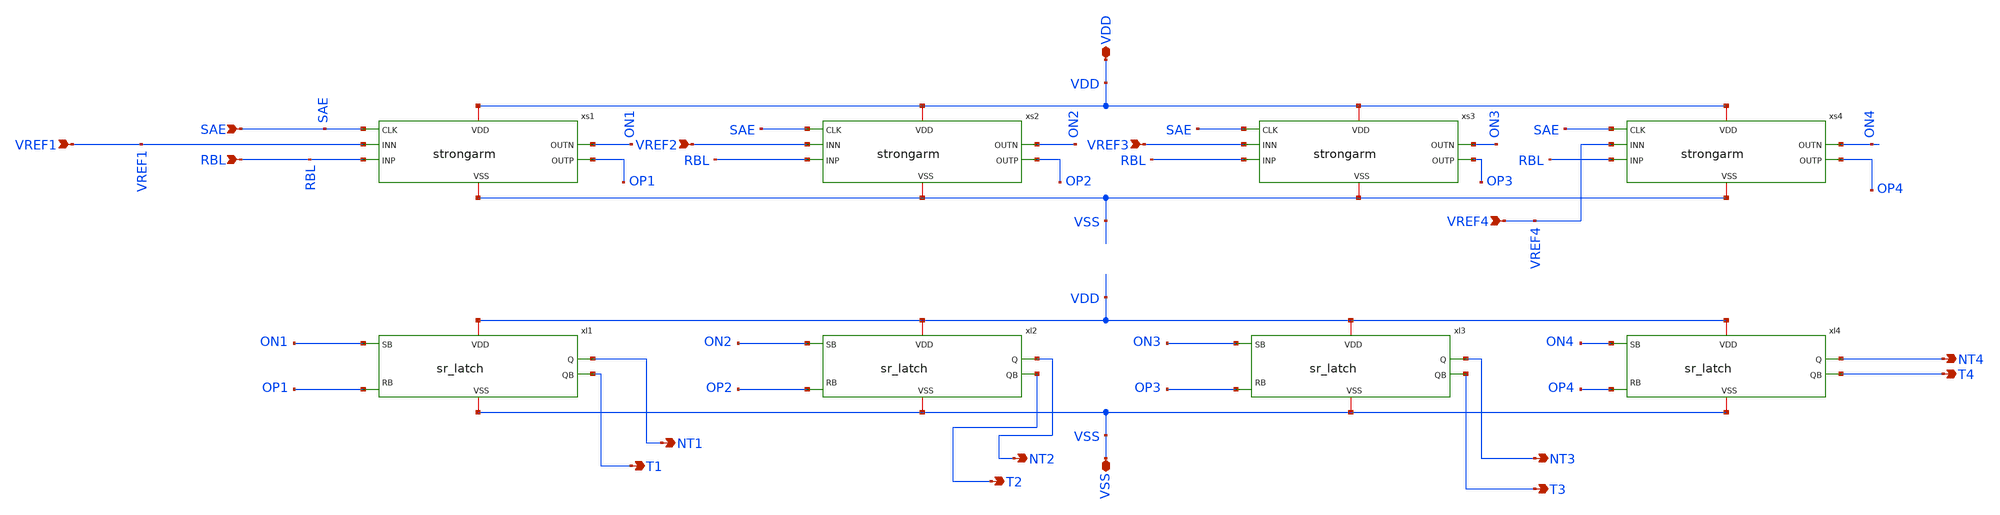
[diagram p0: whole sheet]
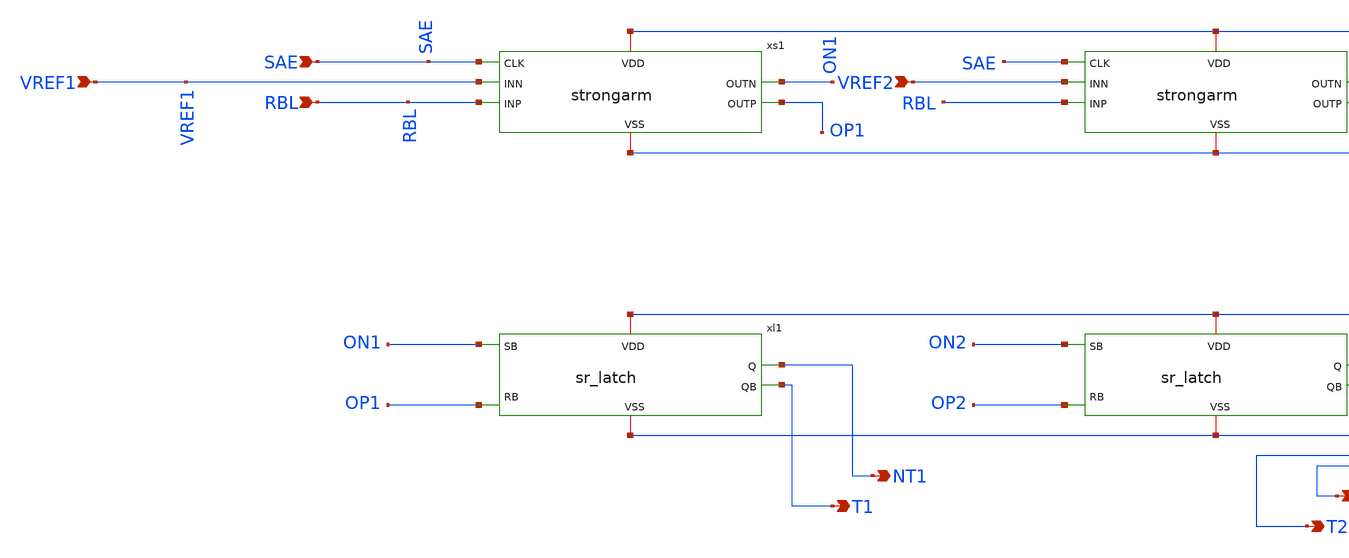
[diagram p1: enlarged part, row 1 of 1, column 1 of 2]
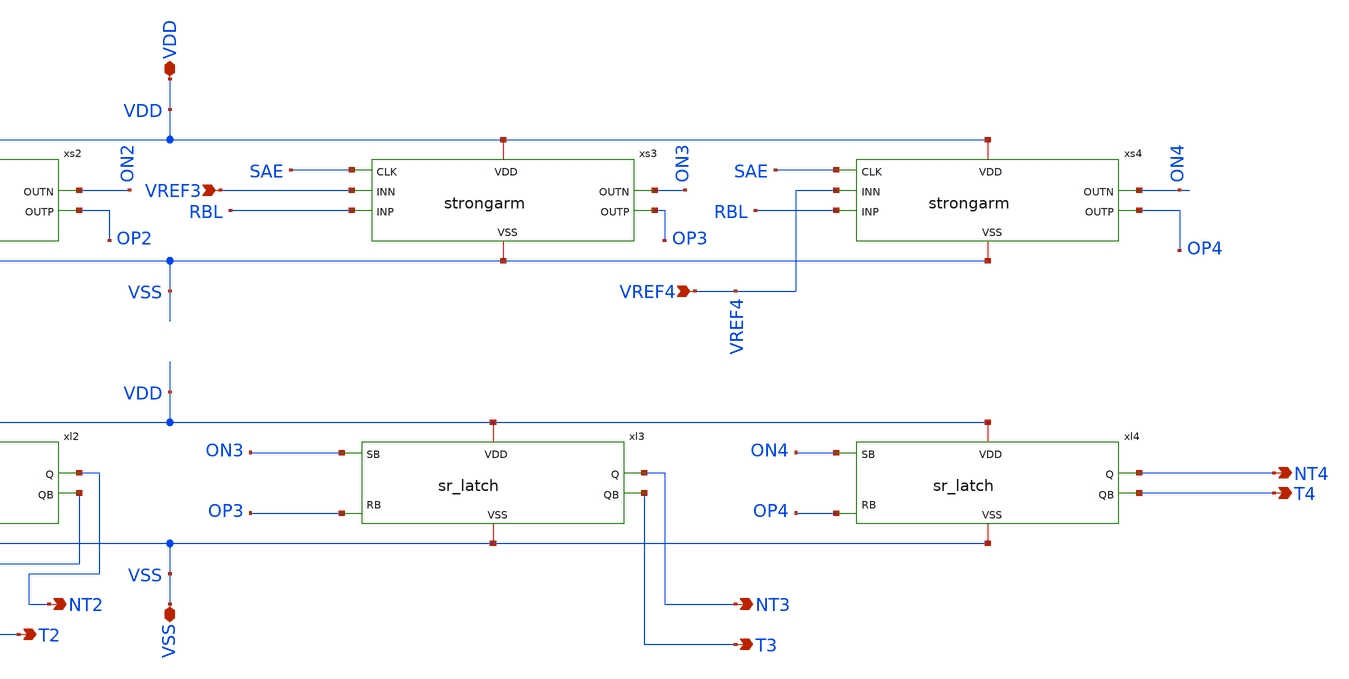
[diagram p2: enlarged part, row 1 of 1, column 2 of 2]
** sch_path: schematics/sense4.sch
**.subckt sense4 SAE RBL VREF1 VREF2 VREF3 VREF4 VDD VSS T1 NT1 NT2 T2 T3 NT3 T4 NT4
*.ipin SAE
*.ipin RBL
*.ipin VREF1
*.ipin VREF2
*.ipin VREF3
*.ipin VREF4
*.iopin VDD
*.iopin VSS
*.opin T1
*.opin NT1
*.opin NT2
*.opin T2
*.opin T3
*.opin NT3
*.opin T4
*.opin NT4
xs1 VDD SAE ON1 OP1 VREF1 RBL VSS strongarm
xs2 VDD SAE ON2 OP2 VREF2 RBL VSS strongarm
xs3 VDD SAE ON3 OP3 VREF3 RBL VSS strongarm
xs4 VDD SAE ON4 OP4 VREF4 RBL VSS strongarm
xl1 VDD ON1 NT1 T1 OP1 VSS sr_latch
xl2 VDD ON2 NT2 T2 OP2 VSS sr_latch
xl3 VDD ON3 NT3 T3 OP3 VSS sr_latch
xl4 VDD ON4 NT4 T4 OP4 VSS sr_latch
**.ends
.end
